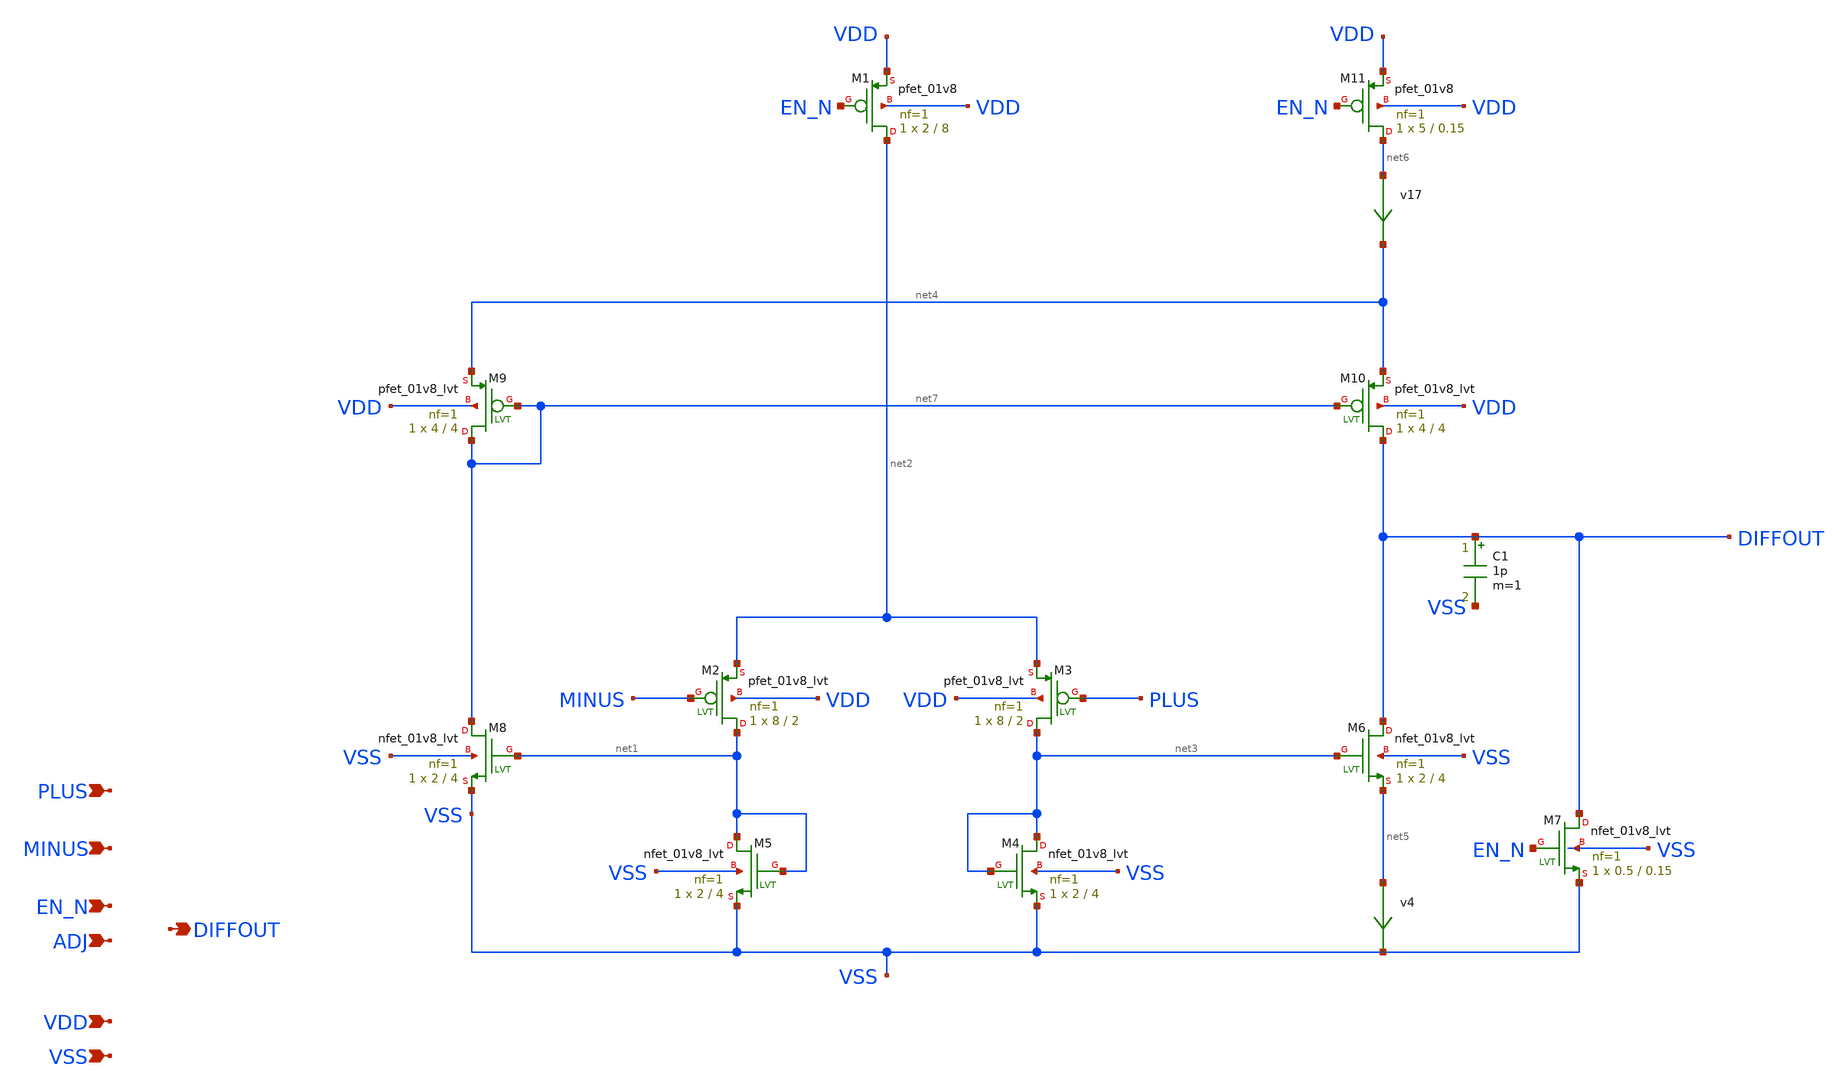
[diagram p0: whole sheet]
** sch_path: projects/pll/trials/opam1.sch
**.subckt opam1 PLUS EN_N VDD VSS MINUS ADJ DIFFOUT
*.ipin PLUS
*.ipin EN_N
*.ipin VDD
*.ipin VSS
*.ipin MINUS
*.ipin ADJ
*.opin DIFFOUT
XM1 net2 EN_N VDD VDD sky130_fd_pr__pfet_01v8 L=8 W=2 nf=1 ad='int((nf+1)/2) * W/nf * 0.29' as='int((nf+2)/2) * W/nf * 0.29'
+ pd='2*int((nf+1)/2) * (W/nf + 0.29)' ps='2*int((nf+2)/2) * (W/nf + 0.29)' nrd='0.29 / W' nrs='0.29 / W'
+ sa=0 sb=0 sd=0 mult=1 m=1
XM2 net1 MINUS net2 VDD sky130_fd_pr__pfet_01v8_lvt L=2 W=8 nf=1 ad='int((nf+1)/2) * W/nf * 0.29' as='int((nf+2)/2) * W/nf * 0.29'
+ pd='2*int((nf+1)/2) * (W/nf + 0.29)' ps='2*int((nf+2)/2) * (W/nf + 0.29)' nrd='0.29 / W' nrs='0.29 / W'
+ sa=0 sb=0 sd=0 mult=1 m=1
XM3 net3 PLUS net2 VDD sky130_fd_pr__pfet_01v8_lvt L=2 W=8 nf=1 ad='int((nf+1)/2) * W/nf * 0.29' as='int((nf+2)/2) * W/nf * 0.29'
+ pd='2*int((nf+1)/2) * (W/nf + 0.29)' ps='2*int((nf+2)/2) * (W/nf + 0.29)' nrd='0.29 / W' nrs='0.29 / W'
+ sa=0 sb=0 sd=0 mult=1 m=1
XM4 net3 net3 VSS VSS sky130_fd_pr__nfet_01v8_lvt L=4 W=2 nf=1 ad='int((nf+1)/2) * W/nf * 0.29' as='int((nf+2)/2) * W/nf * 0.29'
+ pd='2*int((nf+1)/2) * (W/nf + 0.29)' ps='2*int((nf+2)/2) * (W/nf + 0.29)' nrd='0.29 / W' nrs='0.29 / W'
+ sa=0 sb=0 sd=0 mult=1 m=1
XM5 net1 net1 VSS VSS sky130_fd_pr__nfet_01v8_lvt L=4 W=2 nf=1 ad='int((nf+1)/2) * W/nf * 0.29' as='int((nf+2)/2) * W/nf * 0.29'
+ pd='2*int((nf+1)/2) * (W/nf + 0.29)' ps='2*int((nf+2)/2) * (W/nf + 0.29)' nrd='0.29 / W' nrs='0.29 / W'
+ sa=0 sb=0 sd=0 mult=1 m=1
XM6 DIFFOUT net3 net5 VSS sky130_fd_pr__nfet_01v8_lvt L=4 W=2 nf=1 ad='int((nf+1)/2) * W/nf * 0.29' as='int((nf+2)/2) * W/nf * 0.29'
+ pd='2*int((nf+1)/2) * (W/nf + 0.29)' ps='2*int((nf+2)/2) * (W/nf + 0.29)' nrd='0.29 / W' nrs='0.29 / W'
+ sa=0 sb=0 sd=0 mult=1 m=1
XM7 DIFFOUT EN_N VSS VSS sky130_fd_pr__nfet_01v8_lvt L=0.15 W=0.5 nf=1 ad='int((nf+1)/2) * W/nf * 0.29'
+ as='int((nf+2)/2) * W/nf * 0.29' pd='2*int((nf+1)/2) * (W/nf + 0.29)' ps='2*int((nf+2)/2) * (W/nf + 0.29)'
+ nrd='0.29 / W' nrs='0.29 / W' sa=0 sb=0 sd=0 mult=1 m=1
XM8 net7 net1 VSS VSS sky130_fd_pr__nfet_01v8_lvt L=4 W=2 nf=1 ad='int((nf+1)/2) * W/nf * 0.29' as='int((nf+2)/2) * W/nf * 0.29'
+ pd='2*int((nf+1)/2) * (W/nf + 0.29)' ps='2*int((nf+2)/2) * (W/nf + 0.29)' nrd='0.29 / W' nrs='0.29 / W'
+ sa=0 sb=0 sd=0 mult=1 m=1
XM9 net7 net7 net4 VDD sky130_fd_pr__pfet_01v8_lvt L=4 W=4 nf=1 ad='int((nf+1)/2) * W/nf * 0.29' as='int((nf+2)/2) * W/nf * 0.29'
+ pd='2*int((nf+1)/2) * (W/nf + 0.29)' ps='2*int((nf+2)/2) * (W/nf + 0.29)' nrd='0.29 / W' nrs='0.29 / W'
+ sa=0 sb=0 sd=0 mult=1 m=1
XM10 DIFFOUT net7 net4 VDD sky130_fd_pr__pfet_01v8_lvt L=4 W=4 nf=1 ad='int((nf+1)/2) * W/nf * 0.29'
+ as='int((nf+2)/2) * W/nf * 0.29' pd='2*int((nf+1)/2) * (W/nf + 0.29)' ps='2*int((nf+2)/2) * (W/nf + 0.29)'
+ nrd='0.29 / W' nrs='0.29 / W' sa=0 sb=0 sd=0 mult=1 m=1
v4 net5 VSS 0
.save i(v4)
v17 net6 net4 0
.save i(v17)
XM11 net6 EN_N VDD VDD sky130_fd_pr__pfet_01v8 L=0.15 W=5 nf=1 ad='int((nf+1)/2) * W/nf * 0.29' as='int((nf+2)/2) * W/nf * 0.29'
+ pd='2*int((nf+1)/2) * (W/nf + 0.29)' ps='2*int((nf+2)/2) * (W/nf + 0.29)' nrd='0.29 / W' nrs='0.29 / W'
+ sa=0 sb=0 sd=0 mult=1 m=1
C1 DIFFOUT VSS 1p m=1
**.ends
.end
